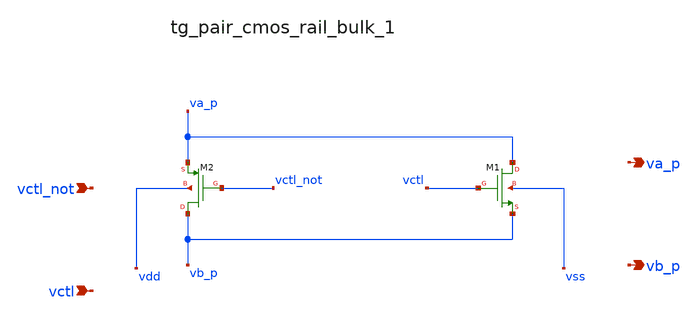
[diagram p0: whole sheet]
** sch_path: analog-db/raw/sw_002_chopper_diff/hier/blocks/tg_pair_cmos_rail_bulk_1.sch
**.subckt tg_pair_cmos_rail_bulk_1 vctl_not vctl va_p vb_p
*.ipin vctl_not
*.ipin vctl
*.opin va_p
*.opin vb_p
XM1 va_p vctl vb_p vss sg13_lv_nmos w=x_dut_xm1_w l=x_dut_xm1_l ng=1 m=x_dut_xm1_m
XM2 vb_p vctl_not va_p vdd sg13_lv_pmos w=x_dut_xm2_w l=x_dut_xm2_l ng=1 m=x_dut_xm2_m
**.ends
.end
